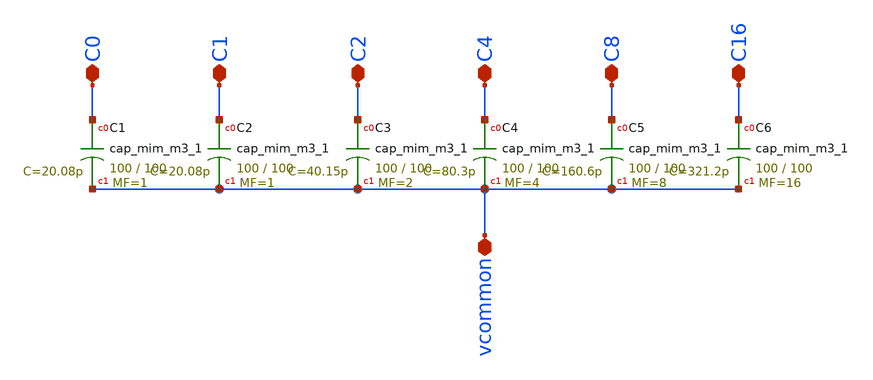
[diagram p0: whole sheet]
** sch_path: caparray.sch
**.subckt caparray C0 C1 C2 C4 C8 C16 vcommon
*.iopin C0
*.iopin C1
*.iopin C2
*.iopin C4
*.iopin C8
*.iopin C16
*.iopin vcommon
XC1 C0 vcommon sky130_fd_pr__cap_mim_m3_1 W=100 L=100 MF=1 m=1
XC2 C1 vcommon sky130_fd_pr__cap_mim_m3_1 W=100 L=100 MF=1 m=1
XC3 C2 vcommon sky130_fd_pr__cap_mim_m3_1 W=100 L=100 MF=2 m=2
XC4 C4 vcommon sky130_fd_pr__cap_mim_m3_1 W=100 L=100 MF=4 m=4
XC5 C8 vcommon sky130_fd_pr__cap_mim_m3_1 W=100 L=100 MF=8 m=8
XC6 C16 vcommon sky130_fd_pr__cap_mim_m3_1 W=100 L=100 MF=16 m=16
**.ends
.end
